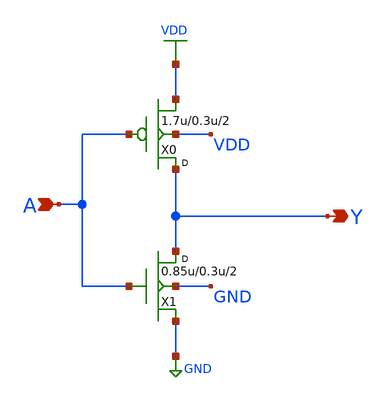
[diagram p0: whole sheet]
** sch_path: openfasoc/common/platforms/gf180osu9t/lib/inv2/gf180mcu_osu_sc_inv_2.sch
**.subckt gf180mcu_osu_sc_inv_2 A Y
*.ipin A
*.opin Y
X0 Y A VDD VDD pmos_3p3 w=1.7u l=0.3u m=2
X1 Y A GND GND nmos_3p3 w=0.85u l=0.3u m=2
**.ends
.GLOBAL VDD
.GLOBAL GND
.end
